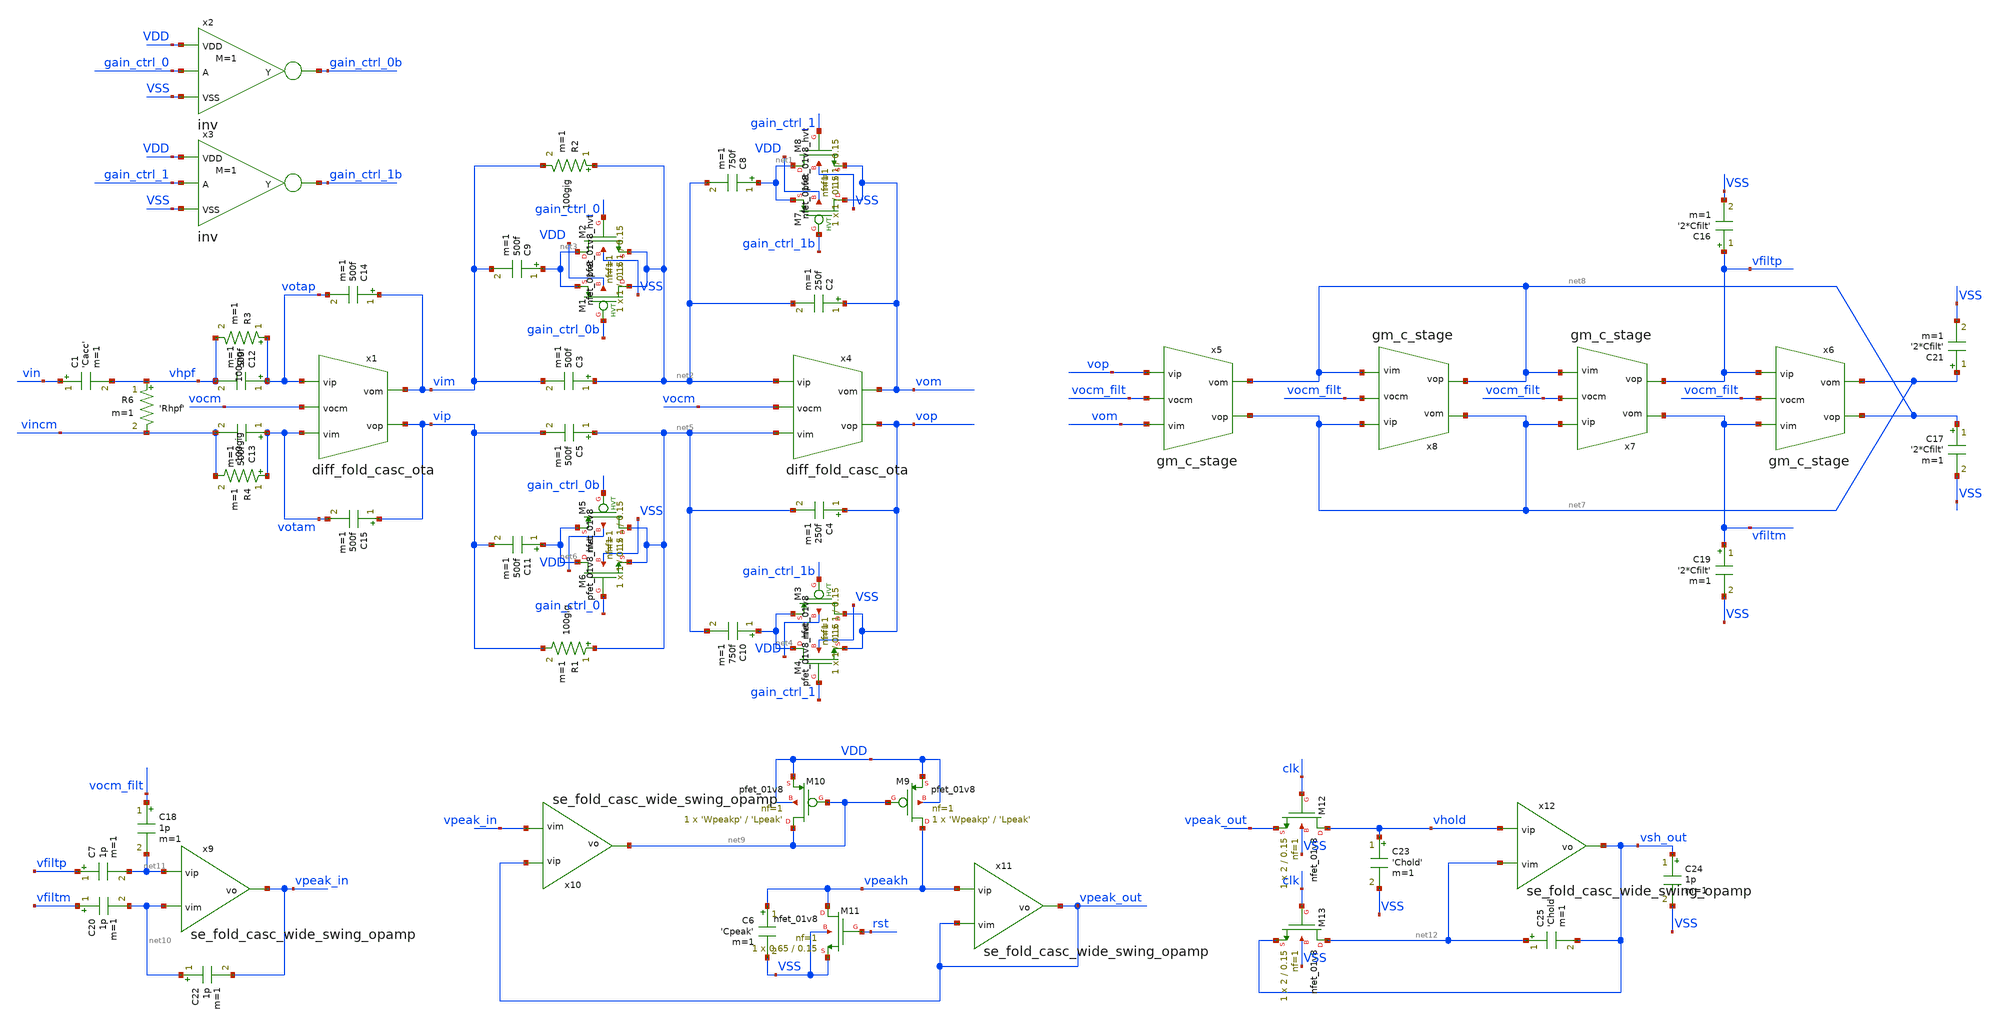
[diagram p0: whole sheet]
** sch_path: designs/amplitude_processing_top_level_lvs.sch
* Copyright 2020 Stefan Frederik Schippers
* Licensed under the Apache License, Version 2.0 (the "License");
* you may not use this file except in compliance with the License.
* You may obtain a copy of the License at
* https://www.apache.org/licenses/LICENSE-2.0
* Unless required by applicable law or agreed to in writing, software
* distributed under the License is distributed on an "AS IS" BASIS,
* WITHOUT WARRANTIES OR CONDITIONS OF ANY KIND, either express or implied.
* See the License for the specific language governing permissions and
* limitations under the License.
**.subckt amplitude_processing_top_level_lvs
C1 vin vhpf 'Cacc' m=1
C2 vom net2 250f m=1
C3 net2 vim 500f m=1
R2 net2 vim 100gig m=1
R6 vhpf vincm 'Rhpf' m=1
XM7 vom gain_ctrl_1b net1 VDD sky130_fd_pr__pfet_01v8_hvt L=0.15 W=1 nf=1 ad='int((nf+1)/2) * W/nf * 0.29'
+ as='int((nf+2)/2) * W/nf * 0.29' pd='2*int((nf+1)/2) * (W/nf + 0.29)' ps='2*int((nf+2)/2) * (W/nf + 0.29)'
+ nrd='0.29 / W' nrs='0.29 / W' sa=0 sb=0 sd=0 mult=1 m=1
XM8 net1 gain_ctrl_1 vom VSS sky130_fd_pr__nfet_01v8 L=0.15 W=1 nf=1 ad='int((nf+1)/2) * W/nf * 0.29'
+ as='int((nf+2)/2) * W/nf * 0.29' pd='2*int((nf+1)/2) * (W/nf + 0.29)' ps='2*int((nf+2)/2) * (W/nf + 0.29)'
+ nrd='0.29 / W' nrs='0.29 / W' sa=0 sb=0 sd=0 mult=1 m=1
C8 net1 net2 750f m=1
XM1 net2 gain_ctrl_0b net3 VDD sky130_fd_pr__pfet_01v8_hvt L=0.15 W=1 nf=1 ad='int((nf+1)/2) * W/nf * 0.29'
+ as='int((nf+2)/2) * W/nf * 0.29' pd='2*int((nf+1)/2) * (W/nf + 0.29)' ps='2*int((nf+2)/2) * (W/nf + 0.29)'
+ nrd='0.29 / W' nrs='0.29 / W' sa=0 sb=0 sd=0 mult=1 m=1
XM2 net3 gain_ctrl_0 net2 VSS sky130_fd_pr__nfet_01v8 L=0.15 W=1 nf=1 ad='int((nf+1)/2) * W/nf * 0.29'
+ as='int((nf+2)/2) * W/nf * 0.29' pd='2*int((nf+1)/2) * (W/nf + 0.29)' ps='2*int((nf+2)/2) * (W/nf + 0.29)'
+ nrd='0.29 / W' nrs='0.29 / W' sa=0 sb=0 sd=0 mult=1 m=1
C9 net3 vim 500f m=1
C4 vop net5 250f m=1
C5 net5 vip 500f m=1
R1 net5 vip 100gig m=1
XM3 vop gain_ctrl_1b net4 VDD sky130_fd_pr__pfet_01v8_hvt L=0.15 W=1 nf=1 ad='int((nf+1)/2) * W/nf * 0.29'
+ as='int((nf+2)/2) * W/nf * 0.29' pd='2*int((nf+1)/2) * (W/nf + 0.29)' ps='2*int((nf+2)/2) * (W/nf + 0.29)'
+ nrd='0.29 / W' nrs='0.29 / W' sa=0 sb=0 sd=0 mult=1 m=1
XM4 net4 gain_ctrl_1 vop VSS sky130_fd_pr__nfet_01v8 L=0.15 W=1 nf=1 ad='int((nf+1)/2) * W/nf * 0.29'
+ as='int((nf+2)/2) * W/nf * 0.29' pd='2*int((nf+1)/2) * (W/nf + 0.29)' ps='2*int((nf+2)/2) * (W/nf + 0.29)'
+ nrd='0.29 / W' nrs='0.29 / W' sa=0 sb=0 sd=0 mult=1 m=1
C10 net4 net5 750f m=1
XM5 net5 gain_ctrl_0b net6 VDD sky130_fd_pr__pfet_01v8_hvt L=0.15 W=1 nf=1 ad='int((nf+1)/2) * W/nf * 0.29'
+ as='int((nf+2)/2) * W/nf * 0.29' pd='2*int((nf+1)/2) * (W/nf + 0.29)' ps='2*int((nf+2)/2) * (W/nf + 0.29)'
+ nrd='0.29 / W' nrs='0.29 / W' sa=0 sb=0 sd=0 mult=1 m=1
XM6 net6 gain_ctrl_0 net5 VSS sky130_fd_pr__nfet_01v8 L=0.15 W=1 nf=1 ad='int((nf+1)/2) * W/nf * 0.29'
+ as='int((nf+2)/2) * W/nf * 0.29' pd='2*int((nf+1)/2) * (W/nf + 0.29)' ps='2*int((nf+2)/2) * (W/nf + 0.29)'
+ nrd='0.29 / W' nrs='0.29 / W' sa=0 sb=0 sd=0 mult=1 m=1
C11 net6 vip 500f m=1
x2 gain_ctrl_0 gain_ctrl_0b VDD VSS inv M=1
x3 gain_ctrl_1 gain_ctrl_1b VDD VSS inv M=1
C12 votap vhpf 500f m=1
C13 votam vincm 500f m=1
C14 vim votap 500f m=1
C15 vip votam 500f m=1
R3 votap vhpf 100gig m=1
R4 votam vincm 100gig m=1
C17 net8 VSS '2*Cfilt' m=1
C21 net7 VSS '2*Cfilt' m=1
C16 vfiltp VSS '2*Cfilt' m=1
C19 vfiltm VSS '2*Cfilt' m=1
x1 vim vip votap votam vocm diff_fold_casc_ota Lbias='Lbias_diff' Ibias=10u Itail=10u Ccomp=2p
x4 vom vop net2 net5 vocm diff_fold_casc_ota Lbias='Lbias_diff' Ibias=10u Itail=10u Ccomp=2p
x5 net8 net7 vop vom vocm_filt gm_c_stage Itail=0.001u Wp=0.5 Wn_diff=8 Wpcm=0.5 Wncm=8 Wn_bias=1
+ Lp=1 Ln_diff=1 Lpcm=1 Lncm=1 Ln_bias=4
x6 net7 net8 vfiltp vfiltm vocm_filt gm_c_stage Itail=0.001u Wp=0.5 Wn_diff=8 Wpcm=0.5 Wncm=8
+ Wn_bias=1 Lp=1 Ln_diff=1 Lpcm=1 Lncm=1 Ln_bias=4
x7 vfiltm vfiltp net7 net8 vocm_filt gm_c_stage Itail=0.001u Wp=0.5 Wn_diff=8 Wpcm=0.5 Wncm=8
+ Wn_bias=1 Lp=1 Ln_diff=1 Lpcm=1 Lncm=1 Ln_bias=4
x8 net7 net8 net7 net8 vocm_filt gm_c_stage Itail=0.001u Wp=0.5 Wn_diff=8 Wpcm=0.5 Wncm=8 Wn_bias=1
+ Lp=1 Ln_diff=1 Lpcm=1 Lncm=1 Ln_bias=4
C6 vpeakh VSS 'Cpeak' m=1
XM9 vpeakh net9 VDD VDD sky130_fd_pr__pfet_01v8 L='Lpeak' W='Wpeakp' nf=1 ad='int((nf+1)/2) * W/nf * 0.29'
+ as='int((nf+2)/2) * W/nf * 0.29' pd='2*int((nf+1)/2) * (W/nf + 0.29)' ps='2*int((nf+2)/2) * (W/nf + 0.29)'
+ nrd='0.29 / W' nrs='0.29 / W' sa=0 sb=0 sd=0 mult=1 m=1
XM10 net9 net9 VDD VDD sky130_fd_pr__pfet_01v8 L='Lpeak' W='Wpeakp' nf=1 ad='int((nf+1)/2) * W/nf * 0.29'
+ as='int((nf+2)/2) * W/nf * 0.29' pd='2*int((nf+1)/2) * (W/nf + 0.29)' ps='2*int((nf+2)/2) * (W/nf + 0.29)'
+ nrd='0.29 / W' nrs='0.29 / W' sa=0 sb=0 sd=0 mult=1 m=1
XM11 vpeakh rst VSS VSS sky130_fd_pr__nfet_01v8 L=0.15 W=0.65 nf=1 ad='int((nf+1)/2) * W/nf * 0.29' as='int((nf+2)/2) * W/nf * 0.29'
+ pd='2*int((nf+1)/2) * (W/nf + 0.29)' ps='2*int((nf+2)/2) * (W/nf + 0.29)' nrd='0.29 / W' nrs='0.29 / W'
+ sa=0 sb=0 sd=0 mult=1 m=1
x9 vpeak_in net11 net10 se_fold_casc_wide_swing_opamp Lbias='Lbias_se' Ibias='Ibias_se'
x10 net9 vpeak_out vpeak_in se_fold_casc_wide_swing_opamp Lbias='Lbias_se' Ibias='Ibias_se'
x11 vpeak_out vpeakh vpeak_out se_fold_casc_wide_swing_opamp Lbias='Lbias_se' Ibias='Ibias_se'
C20 vfiltm net10 1p m=1
C22 net10 vpeak_in 1p m=1
C7 vfiltp net11 1p m=1
C18 vocm_filt net11 1p m=1
XM12 vhold clk vpeak_out VSS sky130_fd_pr__nfet_01v8 L=0.15 W=2 nf=1 ad='int((nf+1)/2) * W/nf * 0.29'
+ as='int((nf+2)/2) * W/nf * 0.29' pd='2*int((nf+1)/2) * (W/nf + 0.29)' ps='2*int((nf+2)/2) * (W/nf + 0.29)'
+ nrd='0.29 / W' nrs='0.29 / W' sa=0 sb=0 sd=0 mult=1 m=1
C23 vhold VSS 'Chold' m=1
C24 vsh_out VSS 1p m=1
XM13 net12 clk vsh_out VSS sky130_fd_pr__nfet_01v8 L=0.15 W=2 nf=1 ad='int((nf+1)/2) * W/nf * 0.29' as='int((nf+2)/2) * W/nf * 0.29'
+ pd='2*int((nf+1)/2) * (W/nf + 0.29)' ps='2*int((nf+2)/2) * (W/nf + 0.29)' nrd='0.29 / W' nrs='0.29 / W'
+ sa=0 sb=0 sd=0 mult=1 m=1
C25 net12 vsh_out 'Chold' m=1
x12 vsh_out vhold net12 se_fold_casc_wide_swing_opamp Lbias='Lbias_se' Ibias='Ibias_se'
**** begin user architecture code

.include $::SKYWATER_MODELS/cells/nfet_01v8/sky130_fd_pr__nfet_01v8__tt.corner.spice
.include $::SKYWATER_MODELS/cells/nfet_01v8_lvt/sky130_fd_pr__nfet_01v8_lvt__tt.corner.spice
.include $::SKYWATER_MODELS/cells/pfet_01v8/sky130_fd_pr__pfet_01v8__tt.corner.spice
.include $::SKYWATER_MODELS/cells/nfet_03v3_nvt/sky130_fd_pr__nfet_03v3_nvt__tt.corner.spice
.include $::SKYWATER_MODELS/cells/nfet_05v0_nvt/sky130_fd_pr__nfet_05v0_nvt__tt.corner.spice
.include $::SKYWATER_MODELS/cells/esd_nfet_01v8/sky130_fd_pr__esd_nfet_01v8__tt.corner.spice
.include $::SKYWATER_MODELS/cells/pfet_01v8_lvt/sky130_fd_pr__pfet_01v8_lvt__tt.corner.spice
.include $::SKYWATER_MODELS/cells/pfet_01v8_hvt/sky130_fd_pr__pfet_01v8_hvt__tt.corner.spice
.include $::SKYWATER_MODELS/cells/esd_pfet_g5v0d10v5/sky130_fd_pr__esd_pfet_g5v0d10v5__tt.corner.spice
.include $::SKYWATER_MODELS/cells/pfet_g5v0d10v5/sky130_fd_pr__pfet_g5v0d10v5__tt.corner.spice
.include $::SKYWATER_MODELS/cells/pfet_g5v0d16v0/sky130_fd_pr__pfet_g5v0d16v0__tt.corner.spice
.include $::SKYWATER_MODELS/cells/nfet_g5v0d10v5/sky130_fd_pr__nfet_g5v0d10v5__tt.corner.spice
.include $::SKYWATER_MODELS/cells/nfet_g5v0d16v0/sky130_fd_pr__nfet_g5v0d16v0__tt_discrete.corner.spice
.include $::SKYWATER_MODELS/cells/esd_nfet_g5v0d10v5/sky130_fd_pr__esd_nfet_g5v0d10v5__tt.corner.spice
.include $::SKYWATER_MODELS/models/corners/tt/nonfet.spice
* Mismatch parameters
.include $::SKYWATER_MODELS/cells/nfet_01v8/sky130_fd_pr__nfet_01v8__mismatch.corner.spice
.include $::SKYWATER_MODELS/cells/pfet_01v8/sky130_fd_pr__pfet_01v8__mismatch.corner.spice
.include $::SKYWATER_MODELS/cells/nfet_01v8_lvt/sky130_fd_pr__nfet_01v8_lvt__mismatch.corner.spice
.include $::SKYWATER_MODELS/cells/pfet_01v8_lvt/sky130_fd_pr__pfet_01v8_lvt__mismatch.corner.spice
.include $::SKYWATER_MODELS/cells/pfet_01v8_hvt/sky130_fd_pr__pfet_01v8_hvt__mismatch.corner.spice
.include $::SKYWATER_MODELS/cells/nfet_g5v0d10v5/sky130_fd_pr__nfet_g5v0d10v5__mismatch.corner.spice
.include $::SKYWATER_MODELS/cells/pfet_g5v0d10v5/sky130_fd_pr__pfet_g5v0d10v5__mismatch.corner.spice
.include $::SKYWATER_MODELS/cells/nfet_05v0_nvt/sky130_fd_pr__nfet_05v0_nvt__mismatch.corner.spice
.include $::SKYWATER_MODELS/cells/nfet_03v3_nvt/sky130_fd_pr__nfet_03v3_nvt__mismatch.corner.spice
* Resistor$::SKYWATER_MODELS/Capacitor
.include $::SKYWATER_MODELS/models/r+c/res_typical__cap_typical.spice
.include $::SKYWATER_MODELS/models/r+c/res_typical__cap_typical__lin.spice
* Special cells
.include $::SKYWATER_MODELS/models/corners/tt/specialized_cells.spice
* All models
.include $::SKYWATER_MODELS/models/all.spice
* Corner
.include $::SKYWATER_MODELS/models/corners/tt/rf.spice

**** end user architecture code
**.ends
**** begin user architecture code

.include amplitude_processing_top_level_lvs_commands.spice

**** end user architecture code
.end
